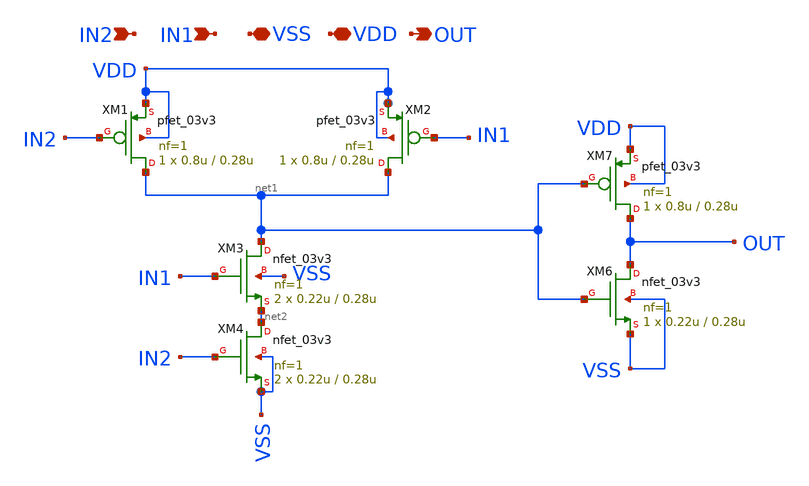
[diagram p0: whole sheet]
** sch_path: Clock_Generator_PAKISTAN_02/xschem/and_2.sch
**.subckt and_2 IN2 IN1 VSS VDD OUT
*.ipin IN2
*.ipin IN1
*.iopin VSS
*.iopin VDD
*.opin OUT
XM7 OUT net1 VDD VDD pfet_03v3 L=0.28u W=0.8u nf=1 ad='int((nf+1)/2) * W/nf * 0.18u' as='int((nf+2)/2) * W/nf * 0.18u'
+ pd='2*int((nf+1)/2) * (W/nf + 0.18u)' ps='2*int((nf+2)/2) * (W/nf + 0.18u)' nrd='0.18u / W' nrs='0.18u / W'
+ sa=0 sb=0 sd=0 m=1
XM6 OUT net1 VSS VSS nfet_03v3 L=0.28u W=0.22u nf=1 ad='int((nf+1)/2) * W/nf * 0.18u' as='int((nf+2)/2) * W/nf * 0.18u'
+ pd='2*int((nf+1)/2) * (W/nf + 0.18u)' ps='2*int((nf+2)/2) * (W/nf + 0.18u)' nrd='0.18u / W' nrs='0.18u / W'
+ sa=0 sb=0 sd=0 m=1
XM1 net1 IN2 VDD VDD pfet_03v3 L=0.28u W=0.8u nf=1 ad='int((nf+1)/2) * W/nf * 0.18u' as='int((nf+2)/2) * W/nf * 0.18u'
+ pd='2*int((nf+1)/2) * (W/nf + 0.18u)' ps='2*int((nf+2)/2) * (W/nf + 0.18u)' nrd='0.18u / W' nrs='0.18u / W'
+ sa=0 sb=0 sd=0 m=1
XM2 net1 IN1 VDD VDD pfet_03v3 L=0.28u W=0.8u nf=1 ad='int((nf+1)/2) * W/nf * 0.18u' as='int((nf+2)/2) * W/nf * 0.18u'
+ pd='2*int((nf+1)/2) * (W/nf + 0.18u)' ps='2*int((nf+2)/2) * (W/nf + 0.18u)' nrd='0.18u / W' nrs='0.18u / W'
+ sa=0 sb=0 sd=0 m=1
XM3 net1 IN1 net2 VSS nfet_03v3 L=0.28u W=0.22u nf=1 ad='int((nf+1)/2) * W/nf * 0.18u' as='int((nf+2)/2) * W/nf * 0.18u'
+ pd='2*int((nf+1)/2) * (W/nf + 0.18u)' ps='2*int((nf+2)/2) * (W/nf + 0.18u)' nrd='0.18u / W' nrs='0.18u / W'
+ sa=0 sb=0 sd=0 m=2
XM4 net2 IN2 VSS VSS nfet_03v3 L=0.28u W=0.22u nf=1 ad='int((nf+1)/2) * W/nf * 0.18u' as='int((nf+2)/2) * W/nf * 0.18u'
+ pd='2*int((nf+1)/2) * (W/nf + 0.18u)' ps='2*int((nf+2)/2) * (W/nf + 0.18u)' nrd='0.18u / W' nrs='0.18u / W'
+ sa=0 sb=0 sd=0 m=2
**.ends
.end
